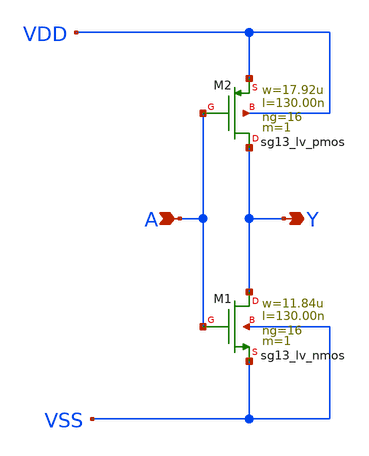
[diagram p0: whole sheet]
** sch_path: ihp-sg13g2/libs.ref/sg13g2_stdcell/sch/xschem/sg13g2_inv_16.sch
* Copyright 2023 IHP PDK Authors
* Licensed under the Apache License, Version 2.0 (the "License");
* you may not use this file except in compliance with the License.
* You may obtain a copy of the License at
* https://www.apache.org/licenses/LICENSE-2.0
* Unless required by applicable law or agreed to in writing, software
* distributed under the License is distributed on an "AS IS" BASIS,
* WITHOUT WARRANTIES OR CONDITIONS OF ANY KIND, either express or implied.
* See the License for the specific language governing permissions and
* limitations under the License.
**.subckt sg13g2_inv_16 Y A
*.opin Y
*.ipin A
XM1 Y A VSS VSS sg13_lv_nmos w=11.84u l=130.00n ng=16 m=1 mm_ok=1
XM2 Y A VDD VDD sg13_lv_pmos w=17.92u l=130.00n ng=16 m=1 mm_ok=1
**.ends
.end
